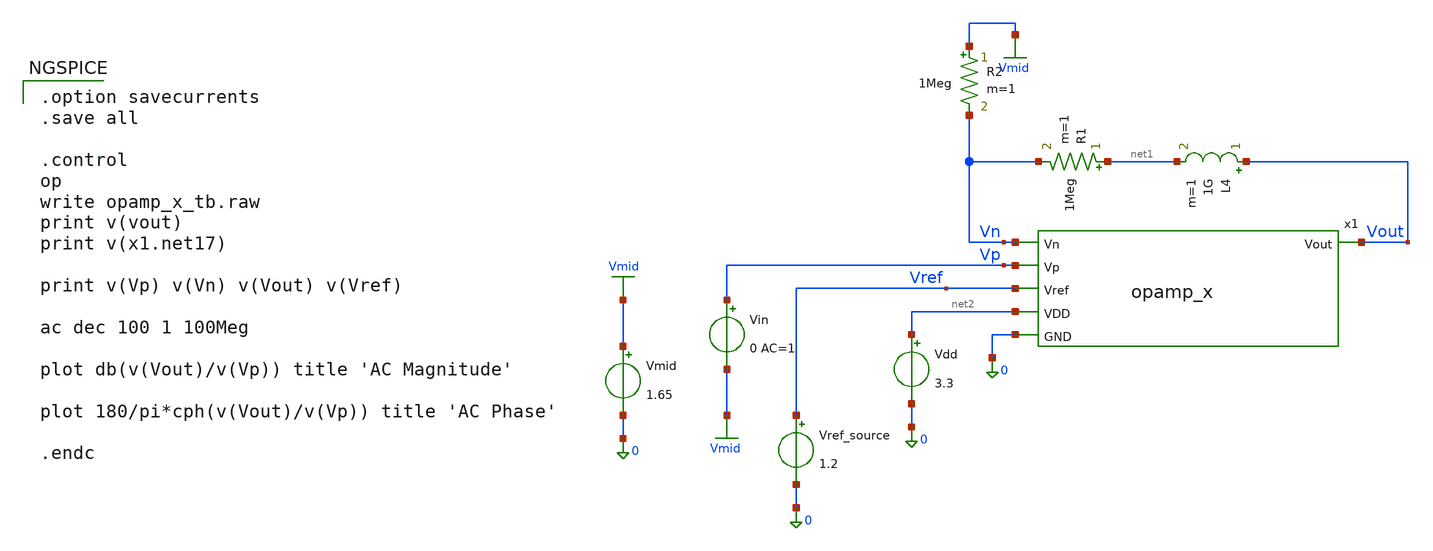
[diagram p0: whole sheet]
** sch_path: xschem/opamp_x_tb.sch
**.subckt opamp_x_tb
x1 net2 Vp Vn Vout Vref 0 opamp_x
Vdd net2 0 3.3
Vref_source Vref 0 1.2
R1 net1 Vn 1Meg m=1
L4 Vout net1 1G m=1
R2 Vmid Vn 1Meg m=1
Vin Vp Vmid 0 AC=1
Vmid Vmid 0 1.65
**** begin user architecture code

** opencircuitdesign pdks install
.lib $::SKYWATER_MODELS/sky130.lib.spice tt


.option savecurrents
.save all

.control
op
write opamp_x_tb.raw
print v(vout)
print v(x1.net17)

print v(Vp) v(Vn) v(Vout) v(Vref)

ac dec 100 1 100Meg

plot db(v(Vout)/v(Vp)) title 'AC Magnitude'

plot 180/pi*cph(v(Vout)/v(Vp)) title 'AC Phase'

.endc

**** end user architecture code
**.ends

* expanding   symbol:  opamp_x.sym # of pins=6
** sym_path: xschem/opamp_x.sym
** sch_path: xschem/opamp_x.sch
.subckt opamp_x VDD Vp Vn Vout Vref GND
*.ipin Vref
*.ipin Vn
*.ipin Vp
*.opin Vout
*.ipin VDD
*.ipin GND
XM1 net3 net3 net1 GND sky130_fd_pr__nfet_g5v0d10v5 L=2 W=10 nf=1 ad='int((1 + 1)/2) * 10 / 1 * 0.29'
+ as='int((1 + 2)/2) * 10 / 1 * 0.29' pd='2*int((1 + 1)/2) * (10 / 1 + 0.29)' ps='2*int((1 + 2)/2) * (10 / 1 + 0.29)'
+ nrd='0.29 / 10 ' nrs='0.29 / 10 ' sa=0 sb=0 sd=0 mult=1 m=1
XM2 net1 net3 GND GND sky130_fd_pr__nfet_g5v0d10v5 L=5 W=5 nf=1 ad='int((1 + 1)/2) * 5 / 1 * 0.29' as='int((1 + 2)/2) * 5 / 1 * 0.29'
+ pd='2*int((1 + 1)/2) * (5 / 1 + 0.29)' ps='2*int((1 + 2)/2) * (5 / 1 + 0.29)' nrd='0.29 / 5 ' nrs='0.29 / 5 '
+ sa=0 sb=0 sd=0 mult=1 m=1
XM3 net2 net3 net4 GND sky130_fd_pr__nfet_g5v0d10v5 L=2 W=10 nf=1 ad='int((1 + 1)/2) * 10 / 1 * 0.29'
+ as='int((1 + 2)/2) * 10 / 1 * 0.29' pd='2*int((1 + 1)/2) * (10 / 1 + 0.29)' ps='2*int((1 + 2)/2) * (10 / 1 + 0.29)'
+ nrd='0.29 / 10 ' nrs='0.29 / 10 ' sa=0 sb=0 sd=0 mult=1 m=1
XM4 net4 net3 GND GND sky130_fd_pr__nfet_g5v0d10v5 L=5 W=5 nf=1 ad='int((1 + 1)/2) * 5 / 1 * 0.29' as='int((1 + 2)/2) * 5 / 1 * 0.29'
+ pd='2*int((1 + 1)/2) * (5 / 1 + 0.29)' ps='2*int((1 + 2)/2) * (5 / 1 + 0.29)' nrd='0.29 / 5 ' nrs='0.29 / 5 '
+ sa=0 sb=0 sd=0 mult=1 m=1
XM5 net5 net2 VDD VDD sky130_fd_pr__pfet_g5v0d10v5 L=5 W=15 nf=1 ad='int((1 + 1)/2) * 15 / 1 * 0.29'
+ as='int((1 + 2)/2) * 15 / 1 * 0.29' pd='2*int((1 + 1)/2) * (15 / 1 + 0.29)' ps='2*int((1 + 2)/2) * (15 / 1 + 0.29)'
+ nrd='0.29 / 15 ' nrs='0.29 / 15 ' sa=0 sb=0 sd=0 mult=1 m=1
XM6 net2 net2 net5 VDD sky130_fd_pr__pfet_g5v0d10v5 L=2 W=20 nf=1 ad='int((1 + 1)/2) * 20 / 1 * 0.29'
+ as='int((1 + 2)/2) * 20 / 1 * 0.29' pd='2*int((1 + 1)/2) * (20 / 1 + 0.29)' ps='2*int((1 + 2)/2) * (20 / 1 + 0.29)'
+ nrd='0.29 / 20 ' nrs='0.29 / 20 ' sa=0 sb=0 sd=0 mult=1 m=1
XM7 net6 net2 VDD VDD sky130_fd_pr__pfet_g5v0d10v5 L=5 W=15 nf=1 ad='int((1 + 1)/2) * 15 / 1 * 0.29'
+ as='int((1 + 2)/2) * 15 / 1 * 0.29' pd='2*int((1 + 1)/2) * (15 / 1 + 0.29)' ps='2*int((1 + 2)/2) * (15 / 1 + 0.29)'
+ nrd='0.29 / 15 ' nrs='0.29 / 15 ' sa=0 sb=0 sd=0 mult=2 m=2
XM8 net7 net2 net6 VDD sky130_fd_pr__pfet_g5v0d10v5 L=2 W=40 nf=1 ad='int((1 + 1)/2) * 40 / 1 * 0.29'
+ as='int((1 + 2)/2) * 40 / 1 * 0.29' pd='2*int((1 + 1)/2) * (40 / 1 + 0.29)' ps='2*int((1 + 2)/2) * (40 / 1 + 0.29)'
+ nrd='0.29 / 40 ' nrs='0.29 / 40 ' sa=0 sb=0 sd=0 mult=1 m=1
XM9 net13 Vp net7 VDD sky130_fd_pr__pfet_g5v0d10v5 L=3 W=20 nf=1 ad='int((1 + 1)/2) * 20 / 1 * 0.29'
+ as='int((1 + 2)/2) * 20 / 1 * 0.29' pd='2*int((1 + 1)/2) * (20 / 1 + 0.29)' ps='2*int((1 + 2)/2) * (20 / 1 + 0.29)'
+ nrd='0.29 / 20 ' nrs='0.29 / 20 ' sa=0 sb=0 sd=0 mult=10 m=10
XM10 net12 Vn net7 VDD sky130_fd_pr__pfet_g5v0d10v5 L=3 W=20 nf=1 ad='int((1 + 1)/2) * 20 / 1 * 0.29'
+ as='int((1 + 2)/2) * 20 / 1 * 0.29' pd='2*int((1 + 1)/2) * (20 / 1 + 0.29)' ps='2*int((1 + 2)/2) * (20 / 1 + 0.29)'
+ nrd='0.29 / 20 ' nrs='0.29 / 20 ' sa=0 sb=0 sd=0 mult=10 m=10
XM11 net10 net9 VDD VDD sky130_fd_pr__pfet_g5v0d10v5 L=5 W=20 nf=1 ad='int((1 + 1)/2) * 20 / 1 * 0.29'
+ as='int((1 + 2)/2) * 20 / 1 * 0.29' pd='2*int((1 + 1)/2) * (20 / 1 + 0.29)' ps='2*int((1 + 2)/2) * (20 / 1 + 0.29)'
+ nrd='0.29 / 20 ' nrs='0.29 / 20 ' sa=0 sb=0 sd=0 mult=5 m=5
XM12 net9 net9 net10 VDD sky130_fd_pr__pfet_g5v0d10v5 L=2 W=20 nf=1 ad='int((1 + 1)/2) * 20 / 1 * 0.29'
+ as='int((1 + 2)/2) * 20 / 1 * 0.29' pd='2*int((1 + 1)/2) * (20 / 1 + 0.29)' ps='2*int((1 + 2)/2) * (20 / 1 + 0.29)'
+ nrd='0.29 / 20 ' nrs='0.29 / 20 ' sa=0 sb=0 sd=0 mult=5 m=5
XM13 net11 net9 VDD VDD sky130_fd_pr__pfet_g5v0d10v5 L=5 W=20 nf=1 ad='int((1 + 1)/2) * 20 / 1 * 0.29'
+ as='int((1 + 2)/2) * 20 / 1 * 0.29' pd='2*int((1 + 1)/2) * (20 / 1 + 0.29)' ps='2*int((1 + 2)/2) * (20 / 1 + 0.29)'
+ nrd='0.29 / 20 ' nrs='0.29 / 20 ' sa=0 sb=0 sd=0 mult=5 m=5
XM14 net18 net9 net11 VDD sky130_fd_pr__pfet_g5v0d10v5 L=2 W=20 nf=1 ad='int((1 + 1)/2) * 20 / 1 * 0.29'
+ as='int((1 + 2)/2) * 20 / 1 * 0.29' pd='2*int((1 + 1)/2) * (20 / 1 + 0.29)' ps='2*int((1 + 2)/2) * (20 / 1 + 0.29)'
+ nrd='0.29 / 20 ' nrs='0.29 / 20 ' sa=0 sb=0 sd=0 mult=5 m=5
XM15 net9 net3 net12 GND sky130_fd_pr__nfet_g5v0d10v5 L=2 W=20 nf=1 ad='int((1 + 1)/2) * 20 / 1 * 0.29'
+ as='int((1 + 2)/2) * 20 / 1 * 0.29' pd='2*int((1 + 1)/2) * (20 / 1 + 0.29)' ps='2*int((1 + 2)/2) * (20 / 1 + 0.29)'
+ nrd='0.29 / 20 ' nrs='0.29 / 20 ' sa=0 sb=0 sd=0 mult=5 m=5
XM16 net12 net3 GND GND sky130_fd_pr__nfet_g5v0d10v5 L=5 W=10 nf=1 ad='int((1 + 1)/2) * 10 / 1 * 0.29'
+ as='int((1 + 2)/2) * 10 / 1 * 0.29' pd='2*int((1 + 1)/2) * (10 / 1 + 0.29)' ps='2*int((1 + 2)/2) * (10 / 1 + 0.29)'
+ nrd='0.29 / 10 ' nrs='0.29 / 10 ' sa=0 sb=0 sd=0 mult=1 m=1
XM17 net17 net3 net13 GND sky130_fd_pr__nfet_g5v0d10v5 L=2 W=20 nf=1 ad='int((1 + 1)/2) * 20 / 1 * 0.29'
+ as='int((1 + 2)/2) * 20 / 1 * 0.29' pd='2*int((1 + 1)/2) * (20 / 1 + 0.29)' ps='2*int((1 + 2)/2) * (20 / 1 + 0.29)'
+ nrd='0.29 / 20 ' nrs='0.29 / 20 ' sa=0 sb=0 sd=0 mult=5 m=5
XM18 net13 net3 GND GND sky130_fd_pr__nfet_g5v0d10v5 L=5 W=10 nf=1 ad='int((1 + 1)/2) * 10 / 1 * 0.29'
+ as='int((1 + 2)/2) * 10 / 1 * 0.29' pd='2*int((1 + 1)/2) * (10 / 1 + 0.29)' ps='2*int((1 + 2)/2) * (10 / 1 + 0.29)'
+ nrd='0.29 / 10 ' nrs='0.29 / 10 ' sa=0 sb=0 sd=0 mult=1 m=1
XM19 net17 net14 net18 VDD sky130_fd_pr__pfet_g5v0d10v5 L=0.5 W=15 nf=1 ad='int((1 + 1)/2) * 15 / 1 * 0.29'
+ as='int((1 + 2)/2) * 15 / 1 * 0.29' pd='2*int((1 + 1)/2) * (15 / 1 + 0.29)' ps='2*int((1 + 2)/2) * (15 / 1 + 0.29)'
+ nrd='0.29 / 15 ' nrs='0.29 / 15 ' sa=0 sb=0 sd=0 mult=10 m=10
XM20 net14 net3 GND GND sky130_fd_pr__nfet_g5v0d10v5 L=5 W=1.5 nf=1 ad='int((1 + 1)/2) * 1.5 / 1 * 0.29'
+ as='int((1 + 2)/2) * 1.5 / 1 * 0.29' pd='2*int((1 + 1)/2) * (1.5 / 1 + 0.29)' ps='2*int((1 + 2)/2) * (1.5 / 1 + 0.29)'
+ nrd='0.29 / 1.5 ' nrs='0.29 / 1.5 ' sa=0 sb=0 sd=0 mult=1 m=1
XM21 net15 net15 VDD VDD sky130_fd_pr__pfet_g5v0d10v5 L=10 W=15 nf=1 ad='int((1 + 1)/2) * 15 / 1 * 0.29'
+ as='int((1 + 2)/2) * 15 / 1 * 0.29' pd='2*int((1 + 1)/2) * (15 / 1 + 0.29)' ps='2*int((1 + 2)/2) * (15 / 1 + 0.29)'
+ nrd='0.29 / 15 ' nrs='0.29 / 15 ' sa=0 sb=0 sd=0 mult=10 m=10
XM22 net14 net14 net15 VDD sky130_fd_pr__pfet_g5v0d10v5 L=10 W=15 nf=1 ad='int((1 + 1)/2) * 15 / 1 * 0.29'
+ as='int((1 + 2)/2) * 15 / 1 * 0.29' pd='2*int((1 + 1)/2) * (15 / 1 + 0.29)' ps='2*int((1 + 2)/2) * (15 / 1 + 0.29)'
+ nrd='0.29 / 15 ' nrs='0.29 / 15 ' sa=0 sb=0 sd=0 mult=10 m=10
XM24 net16 net2 VDD VDD sky130_fd_pr__pfet_g5v0d10v5 L=5 W=4 nf=1 ad='int((1 + 1)/2) * 4 / 1 * 0.29'
+ as='int((1 + 2)/2) * 4 / 1 * 0.29' pd='2*int((1 + 1)/2) * (4 / 1 + 0.29)' ps='2*int((1 + 2)/2) * (4 / 1 + 0.29)'
+ nrd='0.29 / 4 ' nrs='0.29 / 4 ' sa=0 sb=0 sd=0 mult=1 m=1
XM25 net16 net16 net19 GND sky130_fd_pr__nfet_g5v0d10v5 L=0.5 W=15 nf=1 ad='int((1 + 1)/2) * 15 / 1 * 0.29'
+ as='int((1 + 2)/2) * 15 / 1 * 0.29' pd='2*int((1 + 1)/2) * (15 / 1 + 0.29)' ps='2*int((1 + 2)/2) * (15 / 1 + 0.29)'
+ nrd='0.29 / 15 ' nrs='0.29 / 15 ' sa=0 sb=0 sd=0 mult=7 m=7
XM26 net19 net19 GND GND sky130_fd_pr__nfet_g5v0d10v5 L=0.5 W=15 nf=1 ad='int((1 + 1)/2) * 15 / 1 * 0.29'
+ as='int((1 + 2)/2) * 15 / 1 * 0.29' pd='2*int((1 + 1)/2) * (15 / 1 + 0.29)' ps='2*int((1 + 2)/2) * (15 / 1 + 0.29)'
+ nrd='0.29 / 15 ' nrs='0.29 / 15 ' sa=0 sb=0 sd=0 mult=7 m=7
XM27 Vout net18 VDD VDD sky130_fd_pr__pfet_g5v0d10v5 L=0.5 W=20 nf=1 ad='int((1 + 1)/2) * 20 / 1 * 0.29'
+ as='int((1 + 2)/2) * 20 / 1 * 0.29' pd='2*int((1 + 1)/2) * (20 / 1 + 0.29)' ps='2*int((1 + 2)/2) * (20 / 1 + 0.29)'
+ nrd='0.29 / 20 ' nrs='0.29 / 20 ' sa=0 sb=0 sd=0 mult=20 m=20
XM28 Vout net17 GND GND sky130_fd_pr__nfet_g5v0d10v5 L=0.5 W=10 nf=1 ad='int((1 + 1)/2) * 10 / 1 * 0.29'
+ as='int((1 + 2)/2) * 10 / 1 * 0.29' pd='2*int((1 + 1)/2) * (10 / 1 + 0.29)' ps='2*int((1 + 2)/2) * (10 / 1 + 0.29)'
+ nrd='0.29 / 10 ' nrs='0.29 / 10 ' sa=0 sb=0 sd=0 mult=10 m=10
XM33 net11 Vp net8 GND sky130_fd_pr__nfet_g5v0d10v5 L=2 W=20 nf=1 ad='int((1 + 1)/2) * 20 / 1 * 0.29'
+ as='int((1 + 2)/2) * 20 / 1 * 0.29' pd='2*int((1 + 1)/2) * (20 / 1 + 0.29)' ps='2*int((1 + 2)/2) * (20 / 1 + 0.29)'
+ nrd='0.29 / 20 ' nrs='0.29 / 20 ' sa=0 sb=0 sd=0 mult=5 m=5
XM30 net10 Vn net8 GND sky130_fd_pr__nfet_g5v0d10v5 L=2 W=20 nf=1 ad='int((1 + 1)/2) * 20 / 1 * 0.29'
+ as='int((1 + 2)/2) * 20 / 1 * 0.29' pd='2*int((1 + 1)/2) * (20 / 1 + 0.29)' ps='2*int((1 + 2)/2) * (20 / 1 + 0.29)'
+ nrd='0.29 / 20 ' nrs='0.29 / 20 ' sa=0 sb=0 sd=0 mult=5 m=5
XM31 net8 net3 net22 GND sky130_fd_pr__nfet_g5v0d10v5 L=2 W=20 nf=1 ad='int((1 + 1)/2) * 20 / 1 * 0.29'
+ as='int((1 + 2)/2) * 20 / 1 * 0.29' pd='2*int((1 + 1)/2) * (20 / 1 + 0.29)' ps='2*int((1 + 2)/2) * (20 / 1 + 0.29)'
+ nrd='0.29 / 20 ' nrs='0.29 / 20 ' sa=0 sb=0 sd=0 mult=1 m=1
XM32 net22 net3 GND GND sky130_fd_pr__nfet_g5v0d10v5 L=5 W=10 nf=1 ad='int((1 + 1)/2) * 10 / 1 * 0.29'
+ as='int((1 + 2)/2) * 10 / 1 * 0.29' pd='2*int((1 + 1)/2) * (10 / 1 + 0.29)' ps='2*int((1 + 2)/2) * (10 / 1 + 0.29)'
+ nrd='0.29 / 10 ' nrs='0.29 / 10 ' sa=0 sb=0 sd=0 mult=1 m=1
XM23 net18 net16 net17 GND sky130_fd_pr__nfet_g5v0d10v5 L=0.5 W=10 nf=1 ad='int((1 + 1)/2) * 10 / 1 * 0.29'
+ as='int((1 + 2)/2) * 10 / 1 * 0.29' pd='2*int((1 + 1)/2) * (10 / 1 + 0.29)' ps='2*int((1 + 2)/2) * (10 / 1 + 0.29)'
+ nrd='0.29 / 10 ' nrs='0.29 / 10 ' sa=0 sb=0 sd=0 mult=5 m=5
XMr1 net21 Vref GND GND sky130_fd_pr__nfet_g5v0d10v5 L=7 W=5 nf=1 ad='int((1 + 1)/2) * 5 / 1 * 0.29'
+ as='int((1 + 2)/2) * 5 / 1 * 0.29' pd='2*int((1 + 1)/2) * (5 / 1 + 0.29)' ps='2*int((1 + 2)/2) * (5 / 1 + 0.29)'
+ nrd='0.29 / 5 ' nrs='0.29 / 5 ' sa=0 sb=0 sd=0 mult=1 m=1
XMr2 net20 net20 VDD VDD sky130_fd_pr__pfet_g5v0d10v5 L=1 W=1 nf=1 ad='int((1 + 1)/2) * 1 / 1 * 0.29'
+ as='int((1 + 2)/2) * 1 / 1 * 0.29' pd='2*int((1 + 1)/2) * (1 / 1 + 0.29)' ps='2*int((1 + 2)/2) * (1 / 1 + 0.29)'
+ nrd='0.29 / 1 ' nrs='0.29 / 1 ' sa=0 sb=0 sd=0 mult=1 m=1
XMr3 net3 net20 VDD VDD sky130_fd_pr__pfet_g5v0d10v5 L=1 W=1 nf=1 ad='int((1 + 1)/2) * 1 / 1 * 0.29'
+ as='int((1 + 2)/2) * 1 / 1 * 0.29' pd='2*int((1 + 1)/2) * (1 / 1 + 0.29)' ps='2*int((1 + 2)/2) * (1 / 1 + 0.29)'
+ nrd='0.29 / 1 ' nrs='0.29 / 1 ' sa=0 sb=0 sd=0 mult=1 m=1
Vmeas_Iref net20 net21 0
.save i(vmeas_iref)
XC2 Vout net17 sky130_fd_pr__cap_mim_m3_2 W=25 L=25 MF=4 m=4
XC1 net18 Vout sky130_fd_pr__cap_mim_m3_2 W=25 L=25 MF=4 m=4
.ends

.GLOBAL Vmid
.end
